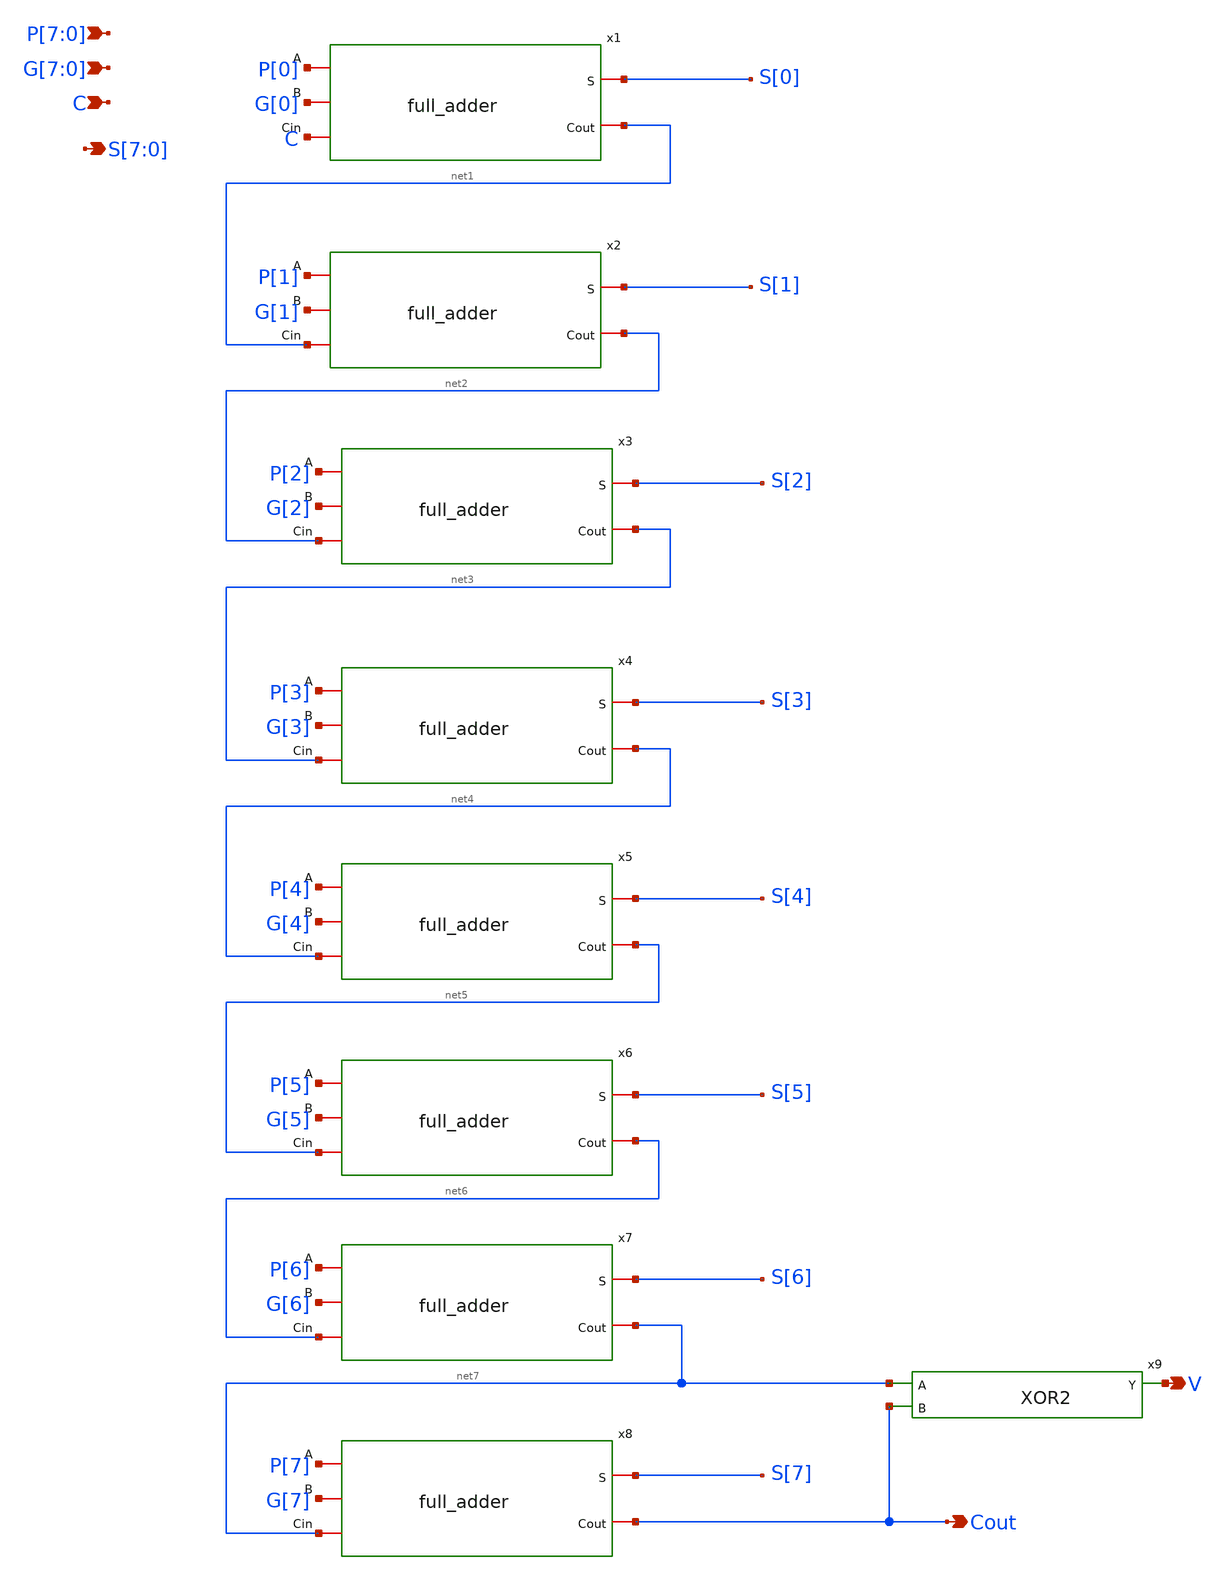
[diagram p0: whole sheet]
** sch_path: design/xschem/ADDER/8-bit_adder.sch
**.subckt 8-bit_adder P[7],P[6],P[5],P[4],P[3],P[2],P[1],P[0]
*+ G[7],G[6],G[5],G[4],G[3],G[2],G[1],G[0] C S[7],S[6],S[5],S[4],S[3],S[2],S[1],S[0] Cout V
*.ipin P[7],P[6],P[5],P[4],P[3],P[2],P[1],P[0]
*.ipin G[7],G[6],G[5],G[4],G[3],G[2],G[1],G[0]
*.ipin C
*.opin S[7],S[6],S[5],S[4],S[3],S[2],S[1],S[0]
*.opin Cout
*.opin V
x1 P[0] S[0] G[0] C net1 full_adder
x2 P[1] S[1] G[1] net1 net2 full_adder
x3 P[2] S[2] G[2] net2 net3 full_adder
x4 P[3] S[3] G[3] net3 net4 full_adder
x5 P[4] S[4] G[4] net4 net5 full_adder
x6 P[5] S[5] G[5] net5 net6 full_adder
x7 P[6] S[6] G[6] net6 net7 full_adder
x8 P[7] S[7] G[7] net7 Cout full_adder
x9 net7 Cout V VSS VDD XOR2
**.ends
.end
